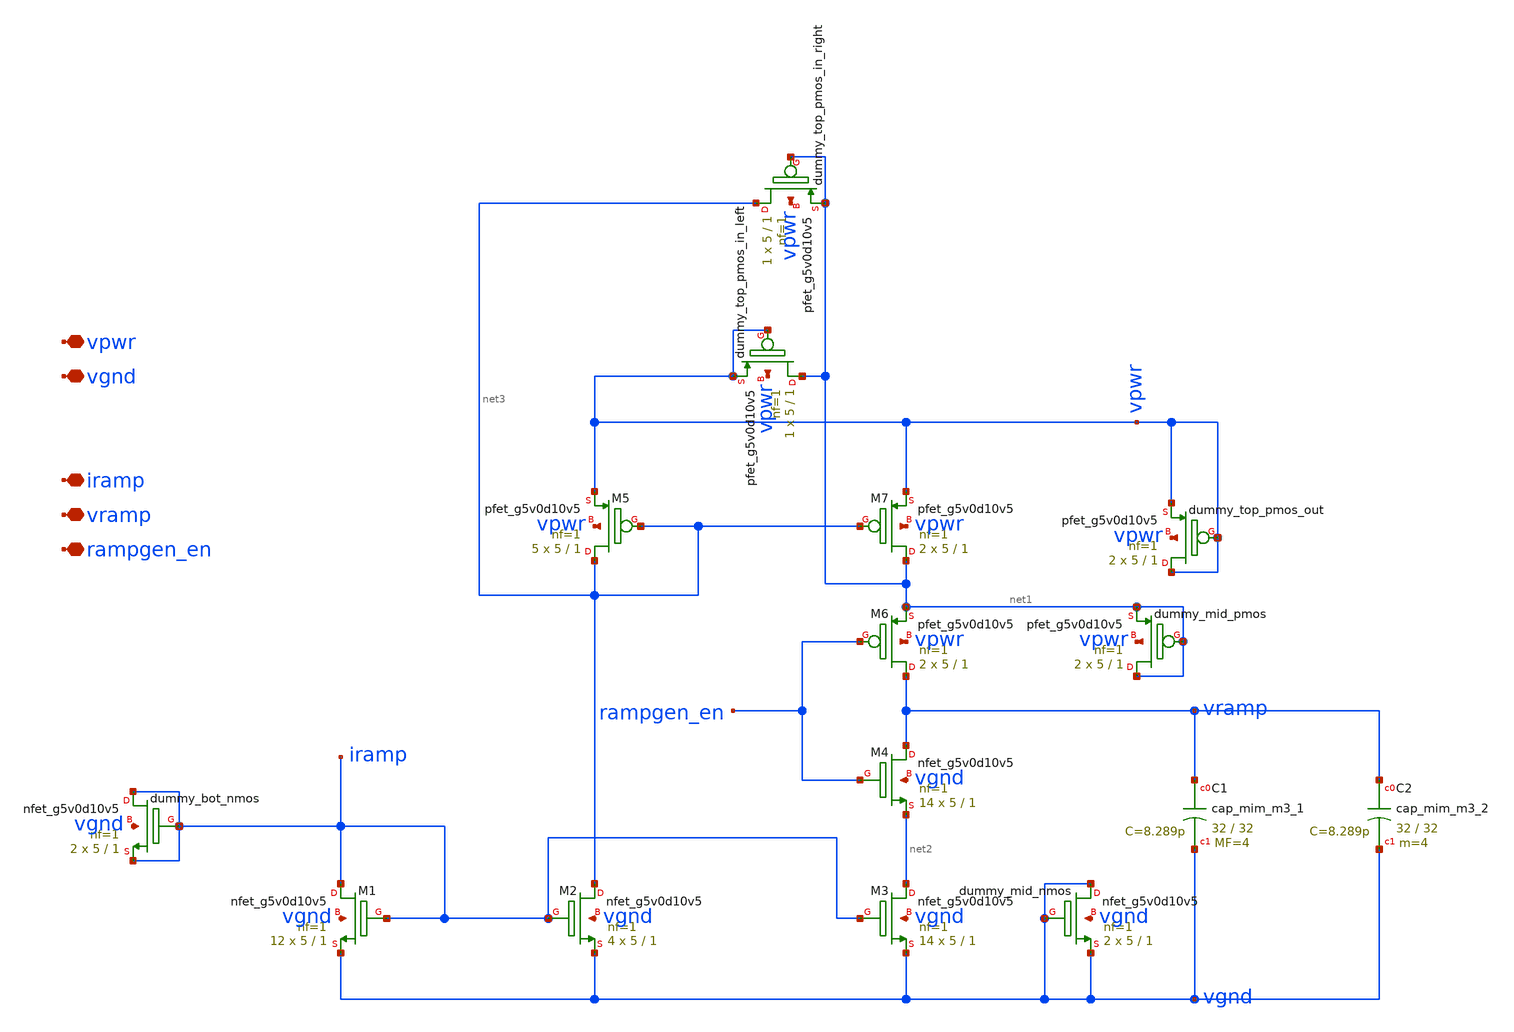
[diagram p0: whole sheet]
** sch_path: images/foss-asic-tools/addons/examples/open-pmic/design/oscillator/rampgen.sch
**.subckt rampgen vpwr vgnd iramp vramp rampgen_en
*.iopin vpwr
*.iopin vgnd
*.iopin iramp
*.iopin vramp
*.iopin rampgen_en
XM1 iramp iramp vgnd vgnd sky130_fd_pr__nfet_g5v0d10v5 L=1 W=5 nf=1 ad='int((nf+1)/2) * W/nf * 0.29'
+ as='int((nf+2)/2) * W/nf * 0.29' pd='2*int((nf+1)/2) * (W/nf + 0.29)' ps='2*int((nf+2)/2) * (W/nf + 0.29)'
+ nrd='0.29 / W' nrs='0.29 / W' sa=0 sb=0 sd=0 mult=12 m=12
XM2 net3 iramp vgnd vgnd sky130_fd_pr__nfet_g5v0d10v5 L=1 W=5 nf=1 ad='int((nf+1)/2) * W/nf * 0.29' as='int((nf+2)/2) * W/nf * 0.29'
+ pd='2*int((nf+1)/2) * (W/nf + 0.29)' ps='2*int((nf+2)/2) * (W/nf + 0.29)' nrd='0.29 / W' nrs='0.29 / W'
+ sa=0 sb=0 sd=0 mult=4 m=4
XM3 net2 iramp vgnd vgnd sky130_fd_pr__nfet_g5v0d10v5 L=1 W=5 nf=1 ad='int((nf+1)/2) * W/nf * 0.29' as='int((nf+2)/2) * W/nf * 0.29'
+ pd='2*int((nf+1)/2) * (W/nf + 0.29)' ps='2*int((nf+2)/2) * (W/nf + 0.29)' nrd='0.29 / W' nrs='0.29 / W'
+ sa=0 sb=0 sd=0 mult=14 m=14
XM4 vramp rampgen_en net2 vgnd sky130_fd_pr__nfet_g5v0d10v5 L=1 W=5 nf=1 ad='int((nf+1)/2) * W/nf * 0.29'
+ as='int((nf+2)/2) * W/nf * 0.29' pd='2*int((nf+1)/2) * (W/nf + 0.29)' ps='2*int((nf+2)/2) * (W/nf + 0.29)'
+ nrd='0.29 / W' nrs='0.29 / W' sa=0 sb=0 sd=0 mult=14 m=14
XM5 net3 net3 vpwr vpwr sky130_fd_pr__pfet_g5v0d10v5 L=1 W=5 nf=1 ad='int((nf+1)/2) * W/nf * 0.29' as='int((nf+2)/2) * W/nf * 0.29'
+ pd='2*int((nf+1)/2) * (W/nf + 0.29)' ps='2*int((nf+2)/2) * (W/nf + 0.29)' nrd='0.29 / W' nrs='0.29 / W'
+ sa=0 sb=0 sd=0 mult=5 m=5
XM6 vramp rampgen_en net1 vpwr sky130_fd_pr__pfet_g5v0d10v5 L=1 W=5 nf=1 ad='int((nf+1)/2) * W/nf * 0.29'
+ as='int((nf+2)/2) * W/nf * 0.29' pd='2*int((nf+1)/2) * (W/nf + 0.29)' ps='2*int((nf+2)/2) * (W/nf + 0.29)'
+ nrd='0.29 / W' nrs='0.29 / W' sa=0 sb=0 sd=0 mult=2 m=2
XM7 net1 net3 vpwr vpwr sky130_fd_pr__pfet_g5v0d10v5 L=1 W=5 nf=1 ad='int((nf+1)/2) * W/nf * 0.29' as='int((nf+2)/2) * W/nf * 0.29'
+ pd='2*int((nf+1)/2) * (W/nf + 0.29)' ps='2*int((nf+2)/2) * (W/nf + 0.29)' nrd='0.29 / W' nrs='0.29 / W'
+ sa=0 sb=0 sd=0 mult=2 m=2
XC1 vramp vgnd sky130_fd_pr__cap_mim_m3_1 W=32 L=32 MF=4 m=4
Xdummy_top_pmos_out vpwr vpwr vpwr vpwr sky130_fd_pr__pfet_g5v0d10v5 L=1 W=5 nf=1 ad='int((nf+1)/2) * W/nf * 0.29'
+ as='int((nf+2)/2) * W/nf * 0.29' pd='2*int((nf+1)/2) * (W/nf + 0.29)' ps='2*int((nf+2)/2) * (W/nf + 0.29)'
+ nrd='0.29 / W' nrs='0.29 / W' sa=0 sb=0 sd=0 mult=2 m=2
Xdummy_mid_pmos net1 net1 net1 vpwr sky130_fd_pr__pfet_g5v0d10v5 L=1 W=5 nf=1 ad='int((nf+1)/2) * W/nf * 0.29'
+ as='int((nf+2)/2) * W/nf * 0.29' pd='2*int((nf+1)/2) * (W/nf + 0.29)' ps='2*int((nf+2)/2) * (W/nf + 0.29)'
+ nrd='0.29 / W' nrs='0.29 / W' sa=0 sb=0 sd=0 mult=2 m=2
Xdummy_mid_nmos vgnd vgnd vgnd vgnd sky130_fd_pr__nfet_g5v0d10v5 L=1 W=5 nf=1 ad='int((nf+1)/2) * W/nf * 0.29'
+ as='int((nf+2)/2) * W/nf * 0.29' pd='2*int((nf+1)/2) * (W/nf + 0.29)' ps='2*int((nf+2)/2) * (W/nf + 0.29)'
+ nrd='0.29 / W' nrs='0.29 / W' sa=0 sb=0 sd=0 mult=2 m=2
Xdummy_bot_nmos iramp iramp iramp vgnd sky130_fd_pr__nfet_g5v0d10v5 L=1 W=5 nf=1 ad='int((nf+1)/2) * W/nf * 0.29'
+ as='int((nf+2)/2) * W/nf * 0.29' pd='2*int((nf+1)/2) * (W/nf + 0.29)' ps='2*int((nf+2)/2) * (W/nf + 0.29)'
+ nrd='0.29 / W' nrs='0.29 / W' sa=0 sb=0 sd=0 mult=2 m=2
Xdummy_top_pmos_in_left net1 vpwr vpwr vpwr sky130_fd_pr__pfet_g5v0d10v5 L=1 W=5 nf=1 ad='int((nf+1)/2) * W/nf * 0.29'
+ as='int((nf+2)/2) * W/nf * 0.29' pd='2*int((nf+1)/2) * (W/nf + 0.29)' ps='2*int((nf+2)/2) * (W/nf + 0.29)'
+ nrd='0.29 / W' nrs='0.29 / W' sa=0 sb=0 sd=0 mult=1 m=1
Xdummy_top_pmos_in_right net3 net1 net1 vpwr sky130_fd_pr__pfet_g5v0d10v5 L=1 W=5 nf=1 ad='int((nf+1)/2) * W/nf * 0.29'
+ as='int((nf+2)/2) * W/nf * 0.29' pd='2*int((nf+1)/2) * (W/nf + 0.29)' ps='2*int((nf+2)/2) * (W/nf + 0.29)'
+ nrd='0.29 / W' nrs='0.29 / W' sa=0 sb=0 sd=0 mult=1 m=1
XC2 vramp vgnd sky130_fd_pr__cap_mim_m3_2 W=32 L=32 MF=4 m=4
**.ends
.end
